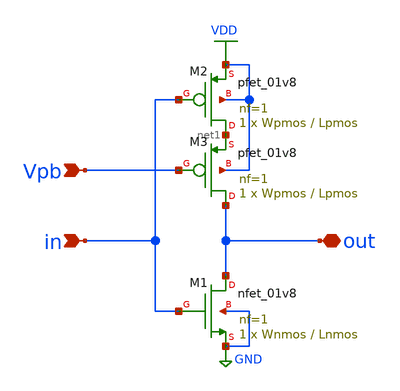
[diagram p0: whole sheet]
** sch_path: xschem/inv/inv_weak_pullup.sch
**.subckt inv_weak_pullup in out Vpb
*.ipin in
*.iopin out
*.ipin Vpb
XM1 out in GND GND sky130_fd_pr__nfet_01v8 L=Lnmos W=Wnmos nf=1 ad='int((nf+1)/2) * W/nf * 0.29' as='int((nf+2)/2) * W/nf * 0.29'
+ pd='2*int((nf+1)/2) * (W/nf + 0.29)' ps='2*int((nf+2)/2) * (W/nf + 0.29)' nrd='0.29 / W' nrs='0.29 / W'
+ sa=0 sb=0 sd=0 mult=1 m=1
XM2 net1 in VDD VDD sky130_fd_pr__pfet_01v8 L=Lpmos W=Wpmos nf=1 ad='int((nf+1)/2) * W/nf * 0.29' as='int((nf+2)/2) * W/nf * 0.29'
+ pd='2*int((nf+1)/2) * (W/nf + 0.29)' ps='2*int((nf+2)/2) * (W/nf + 0.29)' nrd='0.29 / W' nrs='0.29 / W'
+ sa=0 sb=0 sd=0 mult=1 m=1
XM3 out Vpb net1 VDD sky130_fd_pr__pfet_01v8 L=Lpmos W=Wpmos nf=1 ad='int((nf+1)/2) * W/nf * 0.29' as='int((nf+2)/2) * W/nf * 0.29'
+ pd='2*int((nf+1)/2) * (W/nf + 0.29)' ps='2*int((nf+2)/2) * (W/nf + 0.29)' nrd='0.29 / W' nrs='0.29 / W'
+ sa=0 sb=0 sd=0 mult=1 m=1
**.ends
.GLOBAL VDD
.GLOBAL GND
.end
